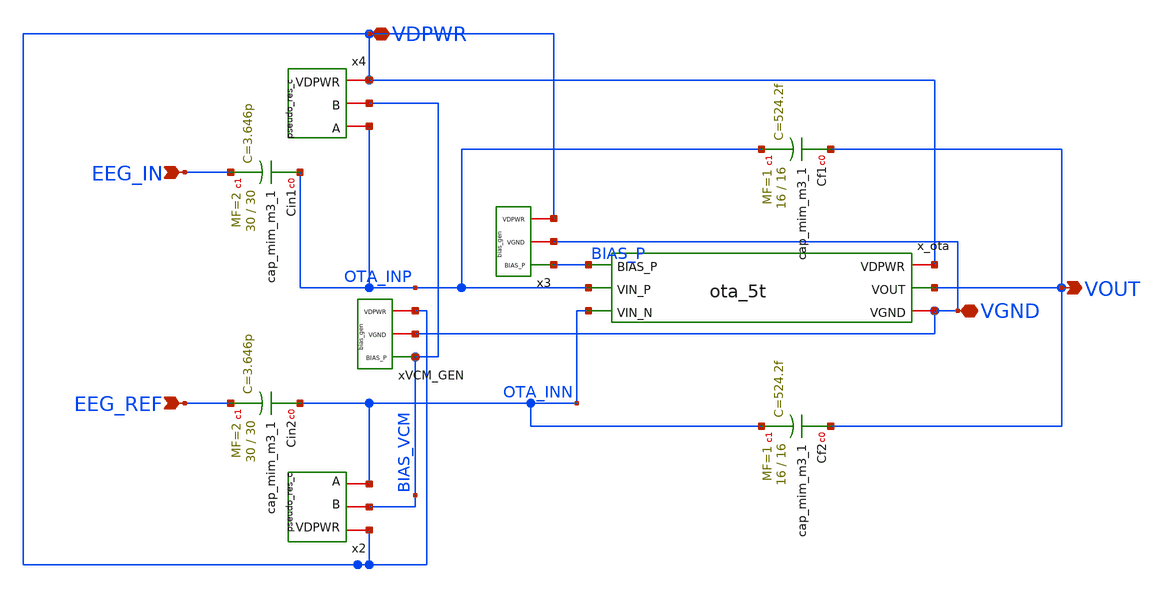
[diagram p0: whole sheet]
** sch_path: xschem/eeg_top.sch
**.subckt eeg_top EEG_IN EEG_REF VDPWR VGND VOUT
*.ipin EEG_IN
*.ipin EEG_REF
*.iopin VDPWR
*.iopin VGND
*.opin VOUT
x_ota BIAS_P VDPWR OTA_INP OTA_INN VOUT VGND ota_5t
x2 VDPWR BIAS_VCM OTA_INN pseudo_res_c
x3 BIAS_P VGND VDPWR bias_gen
x4 VDPWR BIAS_VCM OTA_INP pseudo_res_c
xVCM_GEN BIAS_VCM VGND VDPWR bias_gen
XCin1 OTA_INP EEG_IN sky130_fd_pr__cap_mim_m3_1 W=30 L=30 MF=2 m=2
XCin2 OTA_INN EEG_REF sky130_fd_pr__cap_mim_m3_1 W=30 L=30 MF=2 m=2
XCf1 VOUT OTA_INP sky130_fd_pr__cap_mim_m3_1 W=16 L=16 MF=1 m=1
XCf2 VOUT OTA_INN sky130_fd_pr__cap_mim_m3_1 W=16 L=16 MF=1 m=1
**.ends

* expanding   symbol:  ota_5t.sym # of pins=6
** sym_path: xschem-new/ota_5t.sym
** sch_path: xschem-new/ota_5t.sch
.subckt ota_5t BIAS_P VDPWR VIN_P VIN_N VOUT VGND
*.ipin VIN_P
*.ipin VIN_N
*.ipin BIAS_P
*.iopin VDPWR
*.iopin VGND
*.opin VOUT
XMDIFF_P net1 VIN_P TAIL_P VDPWR sky130_fd_pr__pfet_01v8 L=4 W=48 nf=1 ad='int((1 + 1)/2) * 48 / 1 * 0.29'
+ as='int((1 + 2)/2) * 48 / 1 * 0.29' pd='2*int((1 + 1)/2) * (48 / 1 + 0.29)' ps='2*int((1 + 2)/2) * (48 / 1 + 0.29)'
+ nrd='0.29 / 48 ' nrs='0.29 / 48 ' sa=0 sb=0 sd=0 mult=1 m=1
XMDIFF_N VOUT VIN_N TAIL_P VDPWR sky130_fd_pr__pfet_01v8 L=4 W=48 nf=1 ad='int((1 + 1)/2) * 48 / 1 * 0.29'
+ as='int((1 + 2)/2) * 48 / 1 * 0.29' pd='2*int((1 + 1)/2) * (48 / 1 + 0.29)' ps='2*int((1 + 2)/2) * (48 / 1 + 0.29)'
+ nrd='0.29 / 48 ' nrs='0.29 / 48 ' sa=0 sb=0 sd=0 mult=1 m=1
XMTAIL TAIL_P BIAS_P VDPWR VDPWR sky130_fd_pr__pfet_01v8 L=8 W=0.5 nf=1 ad='int((1 + 1)/2) * 0.5 / 1 * 0.29'
+ as='int((1 + 2)/2) * 0.5 / 1 * 0.29' pd='2*int((1 + 1)/2) * (0.5 / 1 + 0.29)' ps='2*int((1 + 2)/2) * (0.5 / 1 + 0.29)'
+ nrd='0.29 / 0.5 ' nrs='0.29 / 0.5 ' sa=0 sb=0 sd=0 mult=1 m=1
XMLOAD_REF net1 net1 VGND VGND sky130_fd_pr__nfet_01v8 L=16 W=8 nf=1 ad='int((1 + 1)/2) * 8 / 1 * 0.29'
+ as='int((1 + 2)/2) * 8 / 1 * 0.29' pd='2*int((1 + 1)/2) * (8 / 1 + 0.29)' ps='2*int((1 + 2)/2) * (8 / 1 + 0.29)'
+ nrd='0.29 / 8 ' nrs='0.29 / 8 ' sa=0 sb=0 sd=0 mult=1 m=1
XMLOAD_OUT VOUT net1 VGND VGND sky130_fd_pr__nfet_01v8 L=16 W=8 nf=1 ad='int((1 + 1)/2) * 8 / 1 * 0.29'
+ as='int((1 + 2)/2) * 8 / 1 * 0.29' pd='2*int((1 + 1)/2) * (8 / 1 + 0.29)' ps='2*int((1 + 2)/2) * (8 / 1 + 0.29)'
+ nrd='0.29 / 8 ' nrs='0.29 / 8 ' sa=0 sb=0 sd=0 mult=1 m=1
.ends


* expanding   symbol:  pseudo_res_c.sym # of pins=3
** sym_path: xschem/pseudo_res_c.sym
** sch_path: xschem/pseudo_res_c.sch
.subckt pseudo_res_c VDPWR B A
*.iopin A
*.iopin B
*.iopin VDPWR
XP1 A net1 net1 VDPWR sky130_fd_pr__pfet_01v8 L=5 W=0.5 nf=1 ad='int((1 + 1)/2) * 0.5 / 1 * 0.29' as='int((1 + 2)/2) * 0.5 / 1 * 0.29'
+ pd='2*int((1 + 1)/2) * (0.5 / 1 + 0.29)' ps='2*int((1 + 2)/2) * (0.5 / 1 + 0.29)' nrd='0.29 / 0.5 ' nrs='0.29 / 0.5 '
+ sa=0 sb=0 sd=0 mult=10 m=10
XP2 net1 net1 B VDPWR sky130_fd_pr__pfet_01v8 L=5 W=0.5 nf=1 ad='int((1 + 1)/2) * 0.5 / 1 * 0.29' as='int((1 + 2)/2) * 0.5 / 1 * 0.29'
+ pd='2*int((1 + 1)/2) * (0.5 / 1 + 0.29)' ps='2*int((1 + 2)/2) * (0.5 / 1 + 0.29)' nrd='0.29 / 0.5 ' nrs='0.29 / 0.5 '
+ sa=0 sb=0 sd=0 mult=10 m=10
.ends


* expanding   symbol:  bias_gen.sym # of pins=3
** sym_path: xschem/bias_gen.sym
** sch_path: xschem/bias_gen.sch
.subckt bias_gen BIAS_P VGND VDPWR
*.iopin VDPWR
*.iopin VGND
*.opin BIAS_P
XM_BIAS_P BIAS_P BIAS_P VDPWR VDPWR sky130_fd_pr__pfet_01v8 L=2 W=1 nf=1 ad='int((1 + 1)/2) * 1 / 1 * 0.29'
+ as='int((1 + 2)/2) * 1 / 1 * 0.29' pd='2*int((1 + 1)/2) * (1 / 1 + 0.29)' ps='2*int((1 + 2)/2) * (1 / 1 + 0.29)'
+ nrd='0.29 / 1 ' nrs='0.29 / 1 ' sa=0 sb=0 sd=0 mult=1 m=1
XM_BIAS_N BIAS_P BIAS_P VGND VGND sky130_fd_pr__nfet_01v8 L=2 W=0.5 nf=1 ad='int((1 + 1)/2) * 0.5 / 1 * 0.29'
+ as='int((1 + 2)/2) * 0.5 / 1 * 0.29' pd='2*int((1 + 1)/2) * (0.5 / 1 + 0.29)' ps='2*int((1 + 2)/2) * (0.5 / 1 + 0.29)'
+ nrd='0.29 / 0.5 ' nrs='0.29 / 0.5 ' sa=0 sb=0 sd=0 mult=1 m=1
.ends

.end
